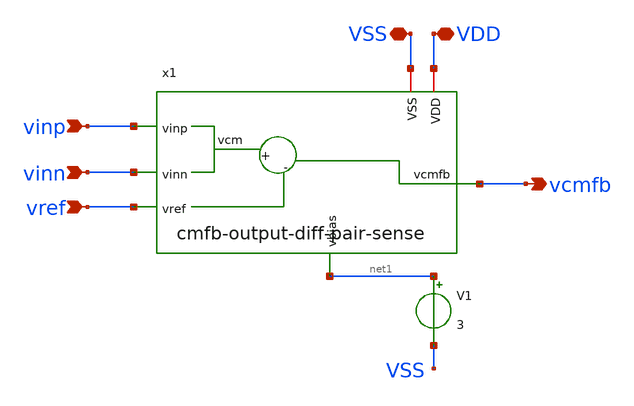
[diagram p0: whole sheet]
** sch_path: analog-db/drawings/shared/cmfb-output-diff-pair-sense-wrapped.sch
* analog-db/drawings/shared/cmfb-output-diff-pair-sense.sch:
* Copyright 2026 MacAnalog Research Group
**.subckt cmfb-output-diff-pair-sense-wrapped VDD vinn VSS vinp vref vcmfb
*.iopin VDD
*.ipin vinn
*.iopin VSS
*.ipin vinp
*.ipin vref
*.opin vcmfb
x1 VSS VDD vinp vinn vcmfb vref net1 cmfb-output-diff-pair-sense
V1 net1 VSS 3
**.ends

* expanding   symbol:  shared/cmfb-output-diff-pair-sense.sym # of pins=7
** sym_path: analog-db/drawings/shared/cmfb-output-diff-pair-sense.sym
** sch_path: analog-db/drawings/shared/cmfb-output-diff-pair-sense.sch
.subckt cmfb-output-diff-pair-sense VSS VDD vinp vinn vcmfb vref vbias
*.iopin VDD
*.ipin vinp
*.ipin vinn
*.ipin vbias
*.opin vcmfb
*.iopin VSS
*.iopin vref
XM4 net1 VDD VDD VDD sg13_lv_pmos w=x_dut_xm4_opamp_rrl_w l=x_dut_xm4_opamp_rrl_l ng=1 m=1 mm_ok=1
XM5 net2 vinn net1 VDD sg13_lv_pmos w=x_dut_xm5_opamp_rrl_w l=x_dut_xm5_opamp_rrl_l ng=1 m=1 mm_ok=1
XM6 vcmfb vref net1 VDD sg13_lv_pmos w=x_dut_xm6_opamp_rrl_w l=x_dut_xm6_opamp_rrl_l ng=1 m=1
+ mm_ok=1
XM7 net2 vinp net1 VDD sg13_lv_pmos w=x_dut_xm7_opamp_rrl_w l=x_dut_xm7_opamp_rrl_l ng=1 m=1 mm_ok=1
XM8 vcmfb vref net1 VDD sg13_lv_pmos w=x_dut_xm8_opamp_rrl_w l=x_dut_xm8_opamp_rrl_l ng=1 m=1
+ mm_ok=1
XM15 vcmfb vcmfb VSS VSS sg13_lv_nmos w=x_dut_xm15_opamp_rrl_w l=x_dut_xm15_opamp_rrl_l ng=1 m=1
+ mm_ok=1
XM16 net2 net2 VSS VSS sg13_lv_nmos w=x_dut_xm16_opamp_rrl_w l=x_dut_xm16_opamp_rrl_l ng=1 m=1
+ mm_ok=1
.ends

.end
